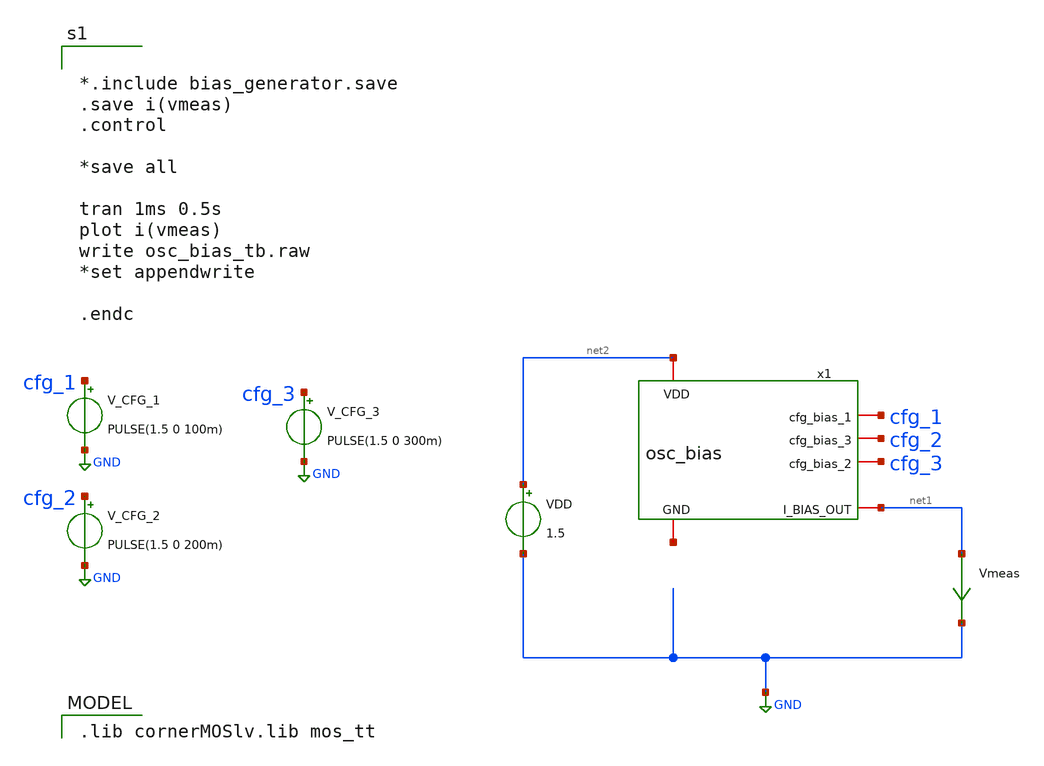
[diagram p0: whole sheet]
** sch_path: osc_bias_tb.sch
**.subckt osc_bias_tb
VDD net2 GND 1.5
Vmeas net1 GND 0
.save i(vmeas)
x1 net2 cfg_1 cfg_2 cfg_3 net3 net1 osc_bias
V_CFG_1 cfg_1 GND PULSE(1.5 0 100m)
V_CFG_2 cfg_2 GND PULSE(1.5 0 200m)
V_CFG_3 cfg_3 GND PULSE(1.5 0 300m)
**** begin user architecture code
 .lib cornerMOSlv.lib mos_tt



*.include bias_generator.save
.save i(vmeas)
.control

*save all

tran 1ms 0.5s
plot i(vmeas)
write osc_bias_tb.raw
*set appendwrite

.endc


**** end user architecture code
**.ends

* expanding   symbol:  osc_bias.sym # of pins=6
** sym_path: osc_bias.sym
** sch_path: osc_bias.sch
.subckt osc_bias VDD cfg_bias_1 cfg_bias_3 cfg_bias_2 GND I_BIAS_OUT
*.iopin VDD
*.iopin GND
*.iopin I_BIAS_OUT
*.iopin cfg_bias_1
*.iopin cfg_bias_2
*.iopin cfg_bias_3
XM1 vp_bias vp_bias VDD VDD sg13_lv_pmos w=1u l=10u ng=1 m=1 mm_ok=1
XM3 vp_bias vp_bias net2 net1 sg13_lv_nmos w=0.25u l=10u ng=1 m=1 mm_ok=1
XM4 net2 net2 net3 net1 sg13_lv_nmos w=0.25u l=10u ng=1 m=1 mm_ok=1
XM5 net3 net3 net1 net1 sg13_lv_nmos w=0.25u l=10u ng=1 m=1 mm_ok=1
XM2 net7 vp_bias VDD VDD sg13_lv_pmos w=0.5u l=10u ng=1 m=1 mm_ok=1
XM6 I_BIAS_OUT cfg_bias_1 net7 VDD sg13_lv_pmos w=0.5u l=5u ng=1 m=1 mm_ok=1
XM7 net4 vp_bias VDD VDD sg13_lv_pmos w=0.5u l=10u ng=1 m=1 mm_ok=1
XM8 net5 vp_bias VDD VDD sg13_lv_pmos w=0.5u l=10u ng=1 m=1 mm_ok=1
XM9 I_BIAS_OUT cfg_bias_2 net4 VDD sg13_lv_pmos w=0.5u l=10u ng=1 m=1 mm_ok=1
XM10 I_BIAS_OUT cfg_bias_3 net5 VDD sg13_lv_pmos w=0.5u l=10u ng=1 m=1 mm_ok=1
XM11 net1 net1 net6 net1 sg13_lv_nmos w=0.25u l=10u ng=1 m=1 mm_ok=1
Vmeas net6 GND 0
.save i(vmeas)
.ends

.GLOBAL GND
.end
